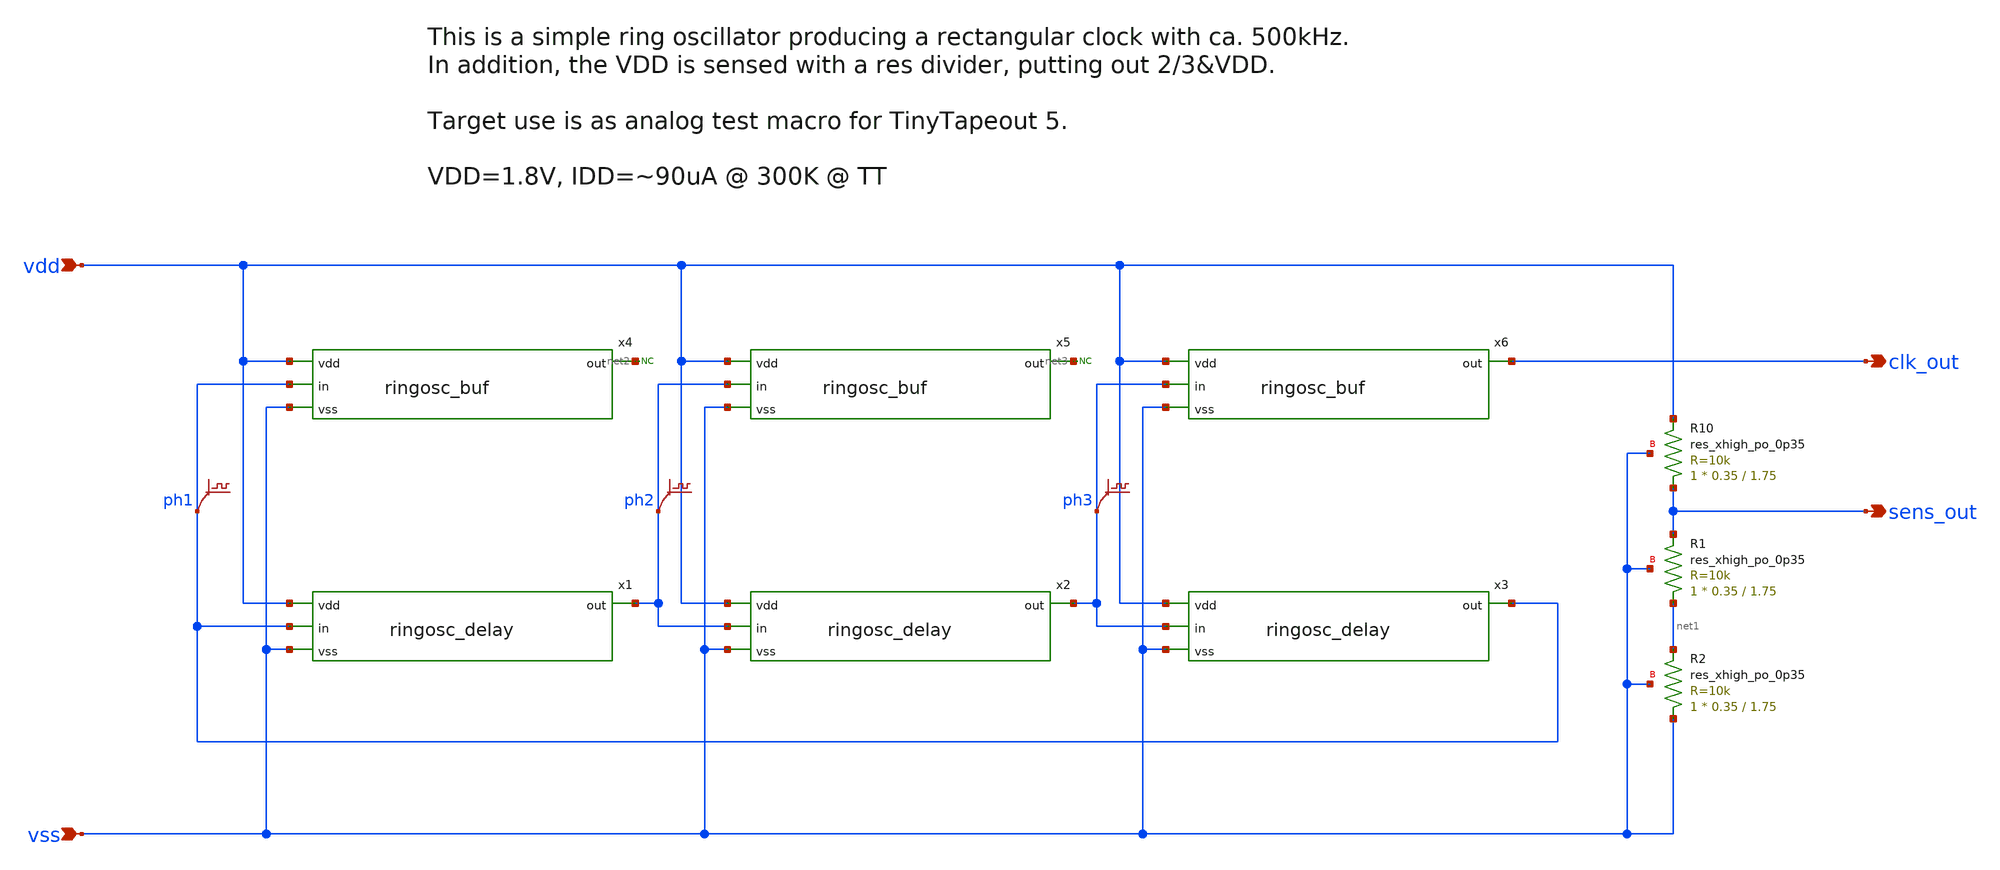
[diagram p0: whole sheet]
** sch_path: xschem/ringosc.sch
**.subckt ringosc vdd vss clk_out sens_out
*.ipin vdd
*.ipin vss
*.opin clk_out
*.opin sens_out
.save v(ph1)
.save v(ph2)
.save v(ph3)
x1 vdd ph1 ph2 vss ringosc_delay
x2 vdd ph2 ph3 vss ringosc_delay
x3 vdd ph3 ph1 vss ringosc_delay
x4 vdd ph1 net2 vss ringosc_buf
x5 vdd ph2 net3 vss ringosc_buf
x6 vdd ph3 clk_out vss ringosc_buf
* noconn #net2
* noconn #net3
XR10 sens_out vdd vss sky130_fd_pr__res_xhigh_po_0p35 L=1.75 mult=1 m=1
XR1 net1 sens_out vss sky130_fd_pr__res_xhigh_po_0p35 L=1.75 mult=1 m=1
XR2 vss net1 vss sky130_fd_pr__res_xhigh_po_0p35 L=1.75 mult=1 m=1
**.ends

* expanding   symbol:  ringosc_delay.sym # of pins=4
** sym_path: xschem/ringosc_delay.sym
** sch_path: xschem/ringosc_delay.sch
.subckt ringosc_delay vdd in out vss
*.ipin vdd
*.ipin vss
*.ipin in
*.opin out
XM1 out in vdd vdd sky130_fd_pr__pfet_01v8 L=10 W=0.5 nf=1 ad='int((nf+1)/2) * W/nf * 0.29' as='int((nf+2)/2) * W/nf * 0.29'
+ pd='2*int((nf+1)/2) * (W/nf + 0.29)' ps='2*int((nf+2)/2) * (W/nf + 0.29)' nrd='0.29 / W' nrs='0.29 / W'
+ sa=0 sb=0 sd=0 mult=1 m=1
XM2 out in net1 vss sky130_fd_pr__nfet_01v8 L=10 W=0.5 nf=1 ad='int((nf+1)/2) * W/nf * 0.29' as='int((nf+2)/2) * W/nf * 0.29'
+ pd='2*int((nf+1)/2) * (W/nf + 0.29)' ps='2*int((nf+2)/2) * (W/nf + 0.29)' nrd='0.29 / W' nrs='0.29 / W'
+ sa=0 sb=0 sd=0 mult=1 m=1
XM4 vss out vss vss sky130_fd_pr__nfet_01v8 L=2 W=10 nf=1 ad='int((nf+1)/2) * W/nf * 0.29' as='int((nf+2)/2) * W/nf * 0.29'
+ pd='2*int((nf+1)/2) * (W/nf + 0.29)' ps='2*int((nf+2)/2) * (W/nf + 0.29)' nrd='0.29 / W' nrs='0.29 / W'
+ sa=0 sb=0 sd=0 mult=1 m=1
XM5 vdd out vdd vdd sky130_fd_pr__pfet_01v8 L=2 W=10 nf=1 ad='int((nf+1)/2) * W/nf * 0.29' as='int((nf+2)/2) * W/nf * 0.29'
+ pd='2*int((nf+1)/2) * (W/nf + 0.29)' ps='2*int((nf+2)/2) * (W/nf + 0.29)' nrd='0.29 / W' nrs='0.29 / W'
+ sa=0 sb=0 sd=0 mult=1 m=1
XM3 net1 in vss vss sky130_fd_pr__nfet_01v8 L=10 W=0.5 nf=1 ad='int((nf+1)/2) * W/nf * 0.29' as='int((nf+2)/2) * W/nf * 0.29'
+ pd='2*int((nf+1)/2) * (W/nf + 0.29)' ps='2*int((nf+2)/2) * (W/nf + 0.29)' nrd='0.29 / W' nrs='0.29 / W'
+ sa=0 sb=0 sd=0 mult=1 m=1
.ends


* expanding   symbol:  ringosc_buf.sym # of pins=4
** sym_path: xschem/ringosc_buf.sym
** sch_path: xschem/ringosc_buf.sch
.subckt ringosc_buf vdd in out vss
*.ipin vdd
*.ipin vss
*.ipin in
*.opin out
XM2 out in vss vss sky130_fd_pr__nfet_01v8 L=0.5 W=10 nf=1 ad='int((nf+1)/2) * W/nf * 0.29' as='int((nf+2)/2) * W/nf * 0.29'
+ pd='2*int((nf+1)/2) * (W/nf + 0.29)' ps='2*int((nf+2)/2) * (W/nf + 0.29)' nrd='0.29 / W' nrs='0.29 / W'
+ sa=0 sb=0 sd=0 mult=1 m=1
XM8 out in vdd vdd sky130_fd_pr__pfet_01v8 L=0.5 W=10 nf=1 ad='int((nf+1)/2) * W/nf * 0.29' as='int((nf+2)/2) * W/nf * 0.29'
+ pd='2*int((nf+1)/2) * (W/nf + 0.29)' ps='2*int((nf+2)/2) * (W/nf + 0.29)' nrd='0.29 / W' nrs='0.29 / W'
+ sa=0 sb=0 sd=0 mult=1 m=1
XM1 out in vdd vdd sky130_fd_pr__pfet_01v8 L=0.5 W=10 nf=1 ad='int((nf+1)/2) * W/nf * 0.29' as='int((nf+2)/2) * W/nf * 0.29'
+ pd='2*int((nf+1)/2) * (W/nf + 0.29)' ps='2*int((nf+2)/2) * (W/nf + 0.29)' nrd='0.29 / W' nrs='0.29 / W'
+ sa=0 sb=0 sd=0 mult=1 m=1
.ends

.end
